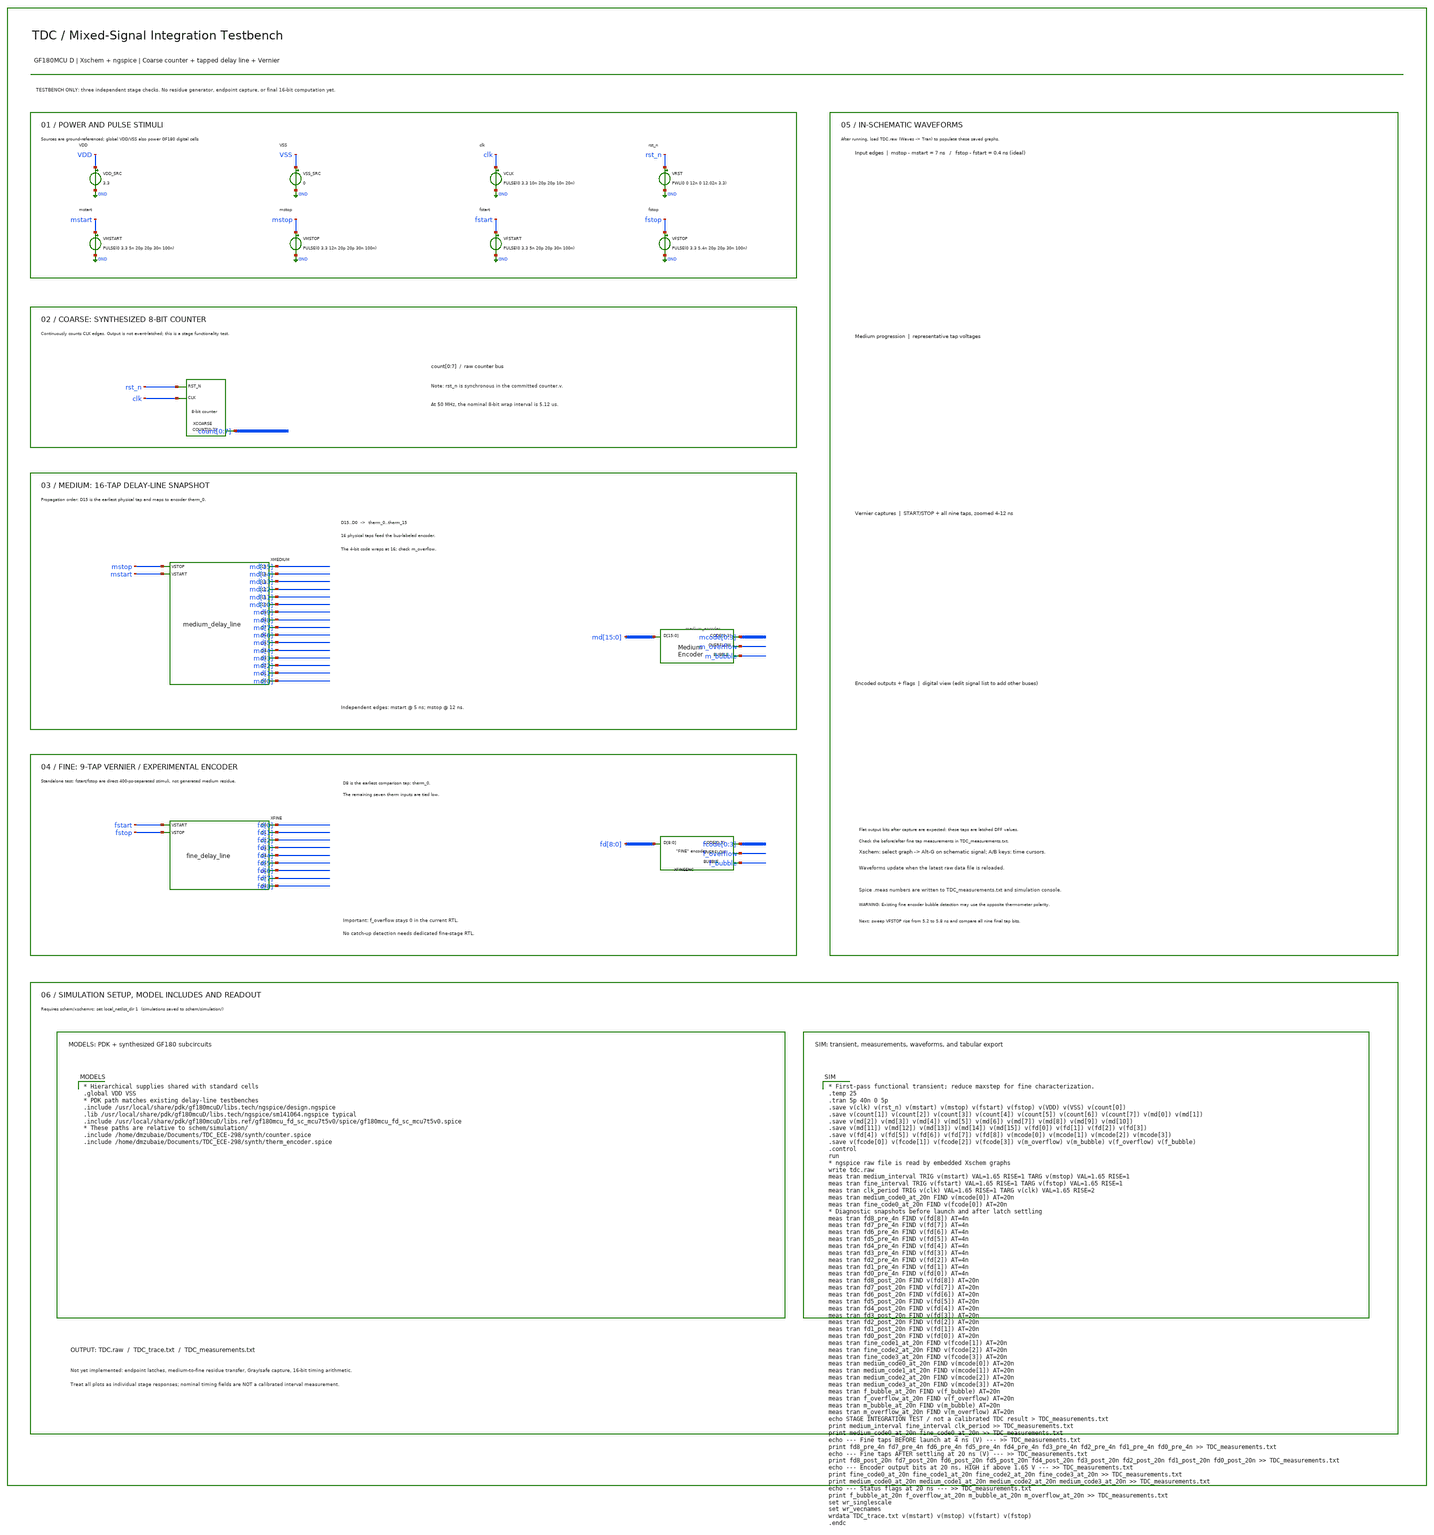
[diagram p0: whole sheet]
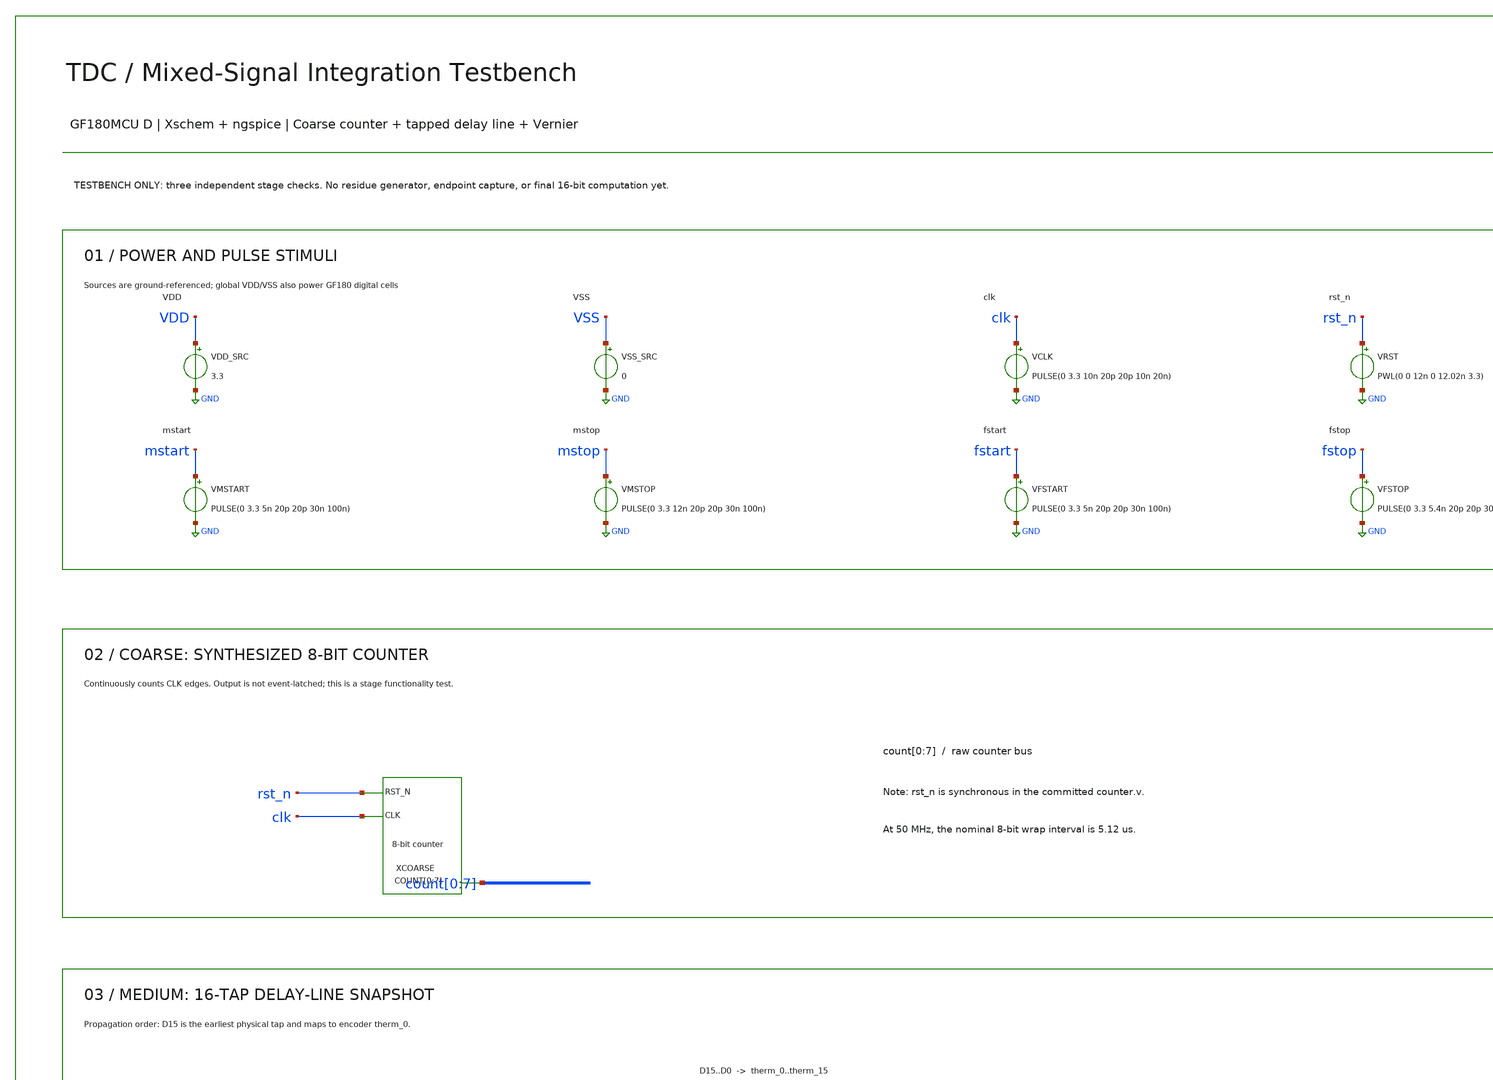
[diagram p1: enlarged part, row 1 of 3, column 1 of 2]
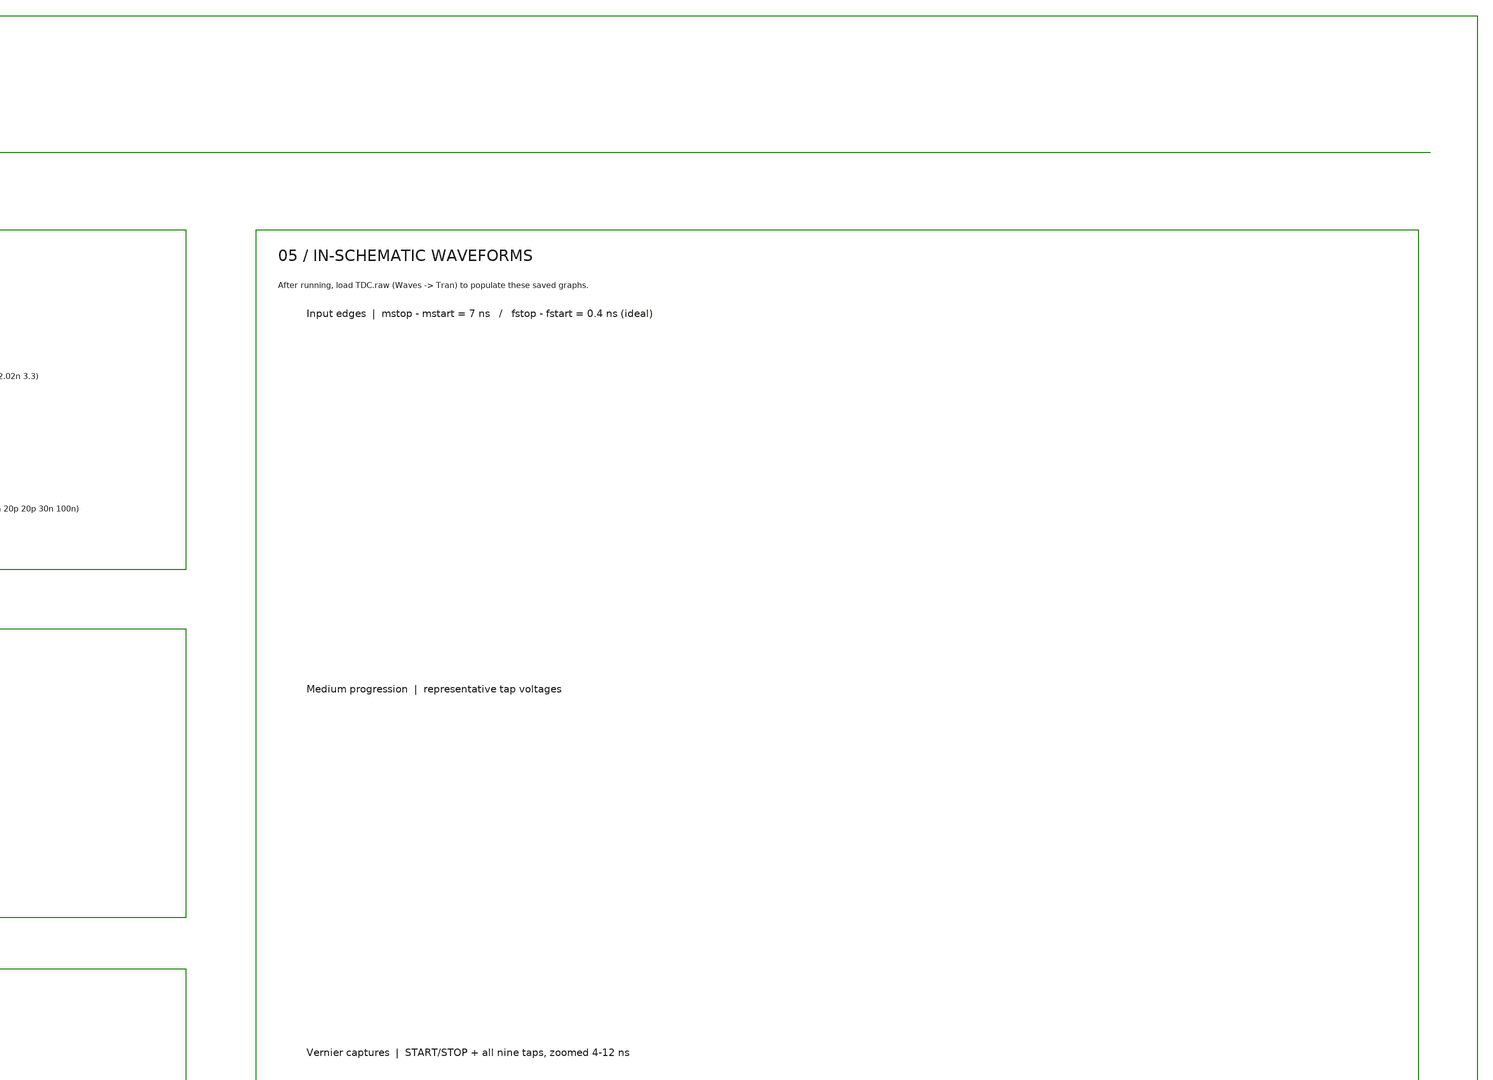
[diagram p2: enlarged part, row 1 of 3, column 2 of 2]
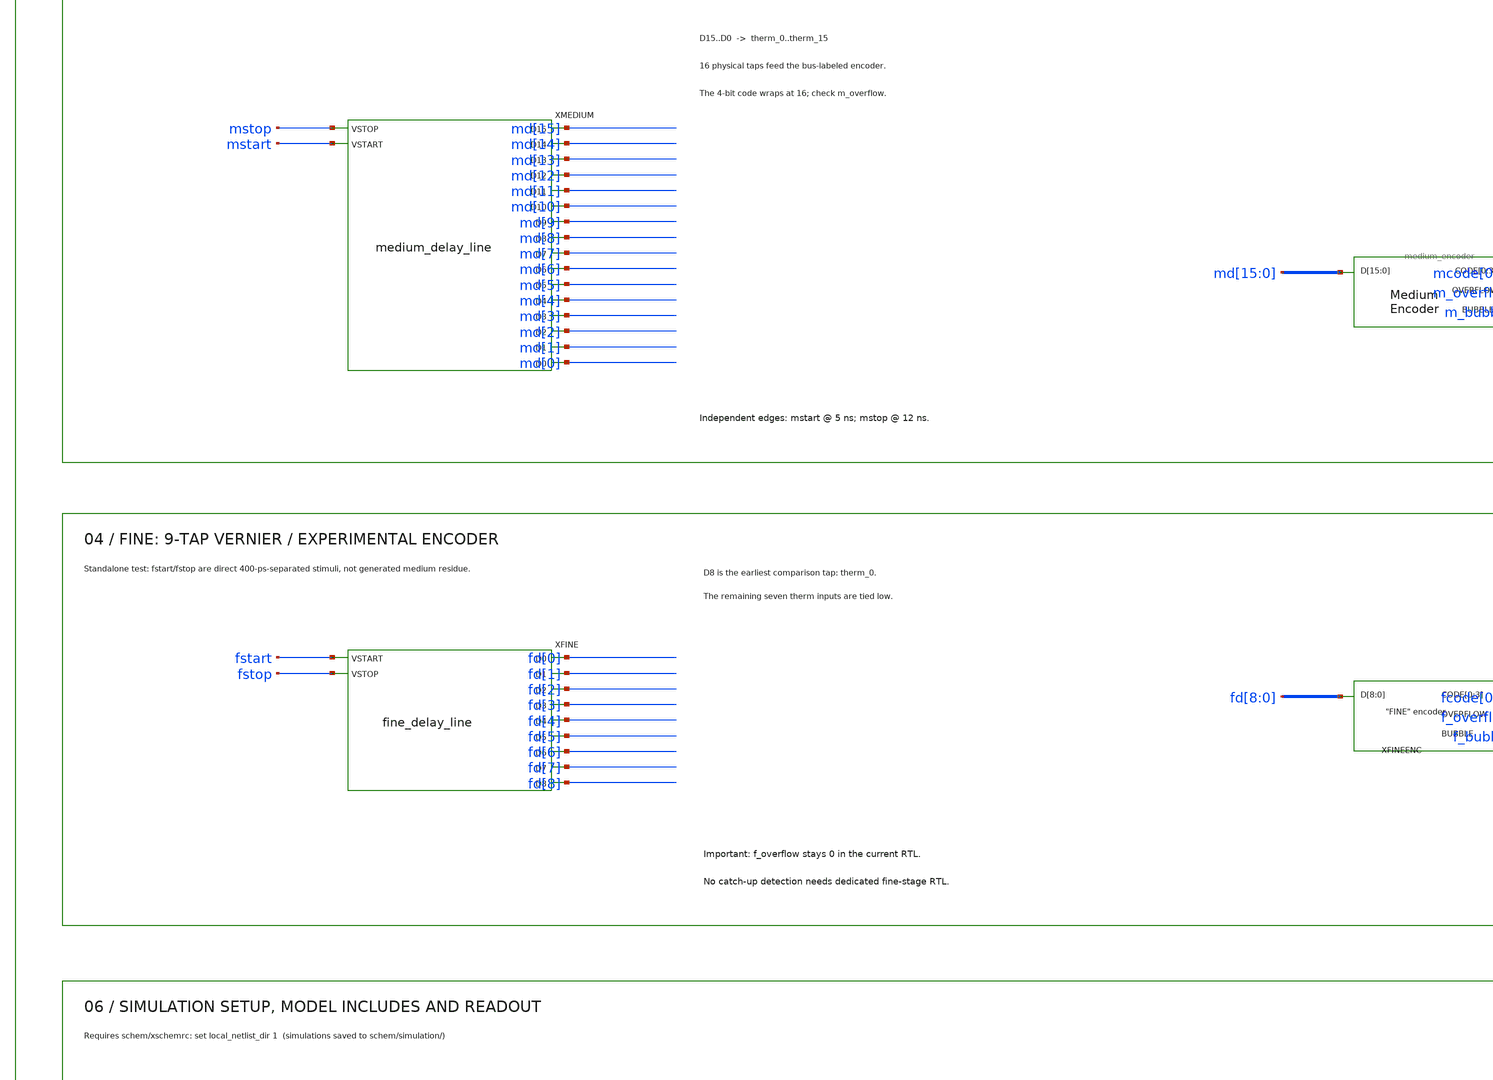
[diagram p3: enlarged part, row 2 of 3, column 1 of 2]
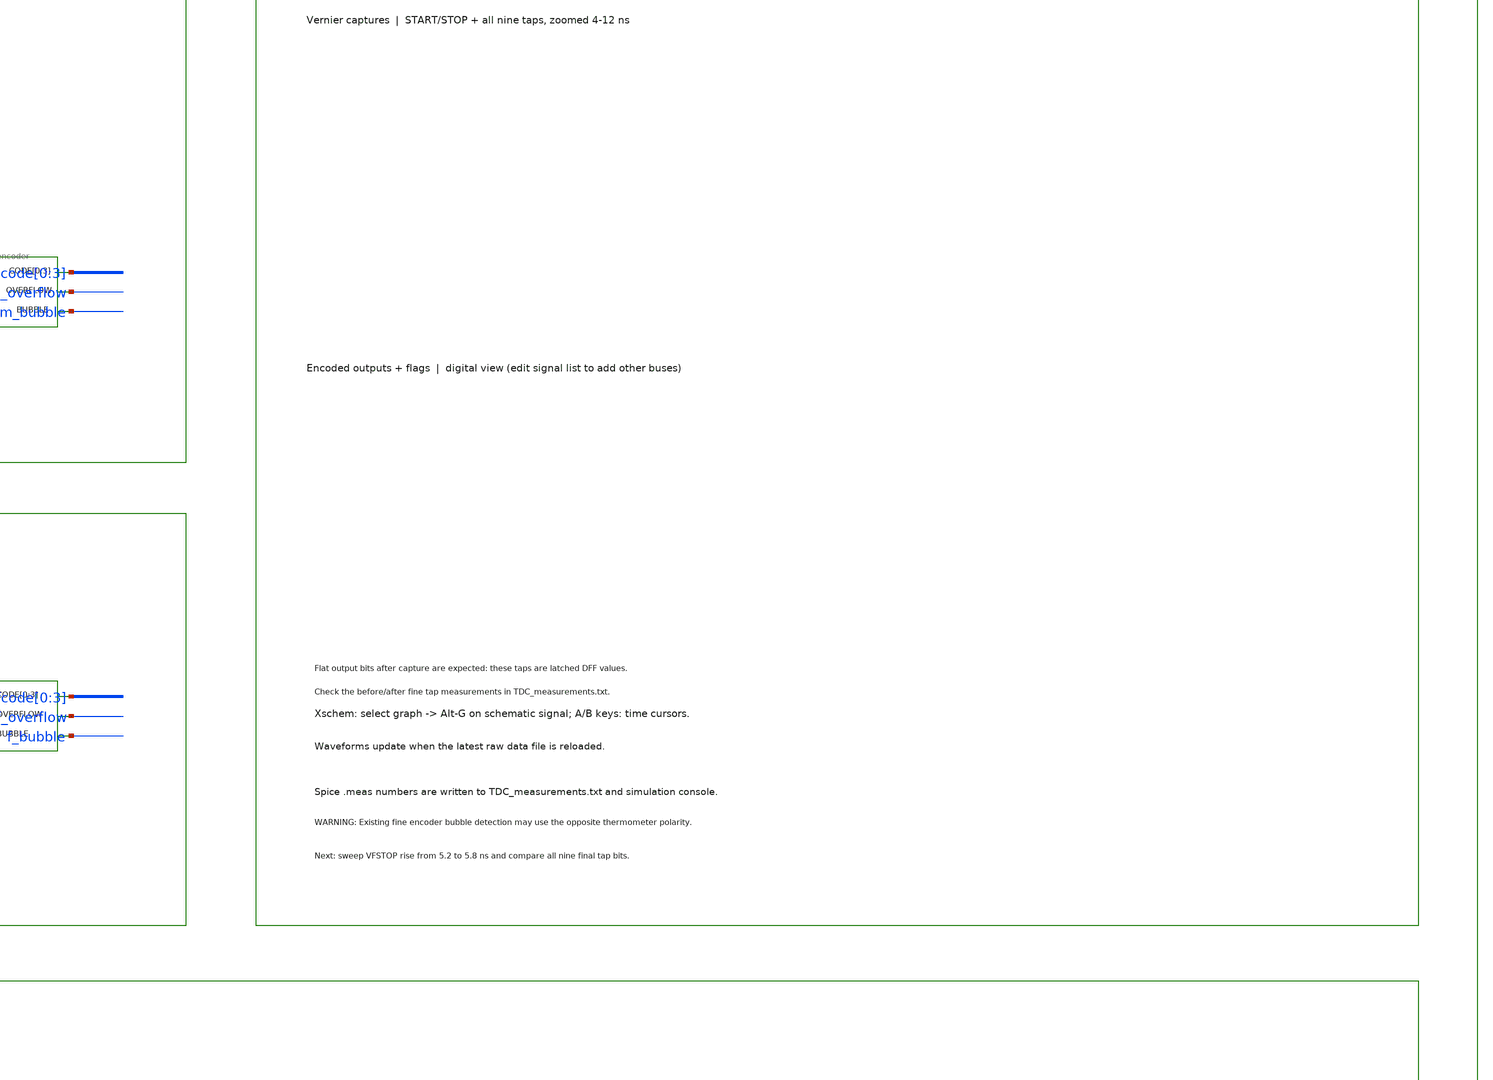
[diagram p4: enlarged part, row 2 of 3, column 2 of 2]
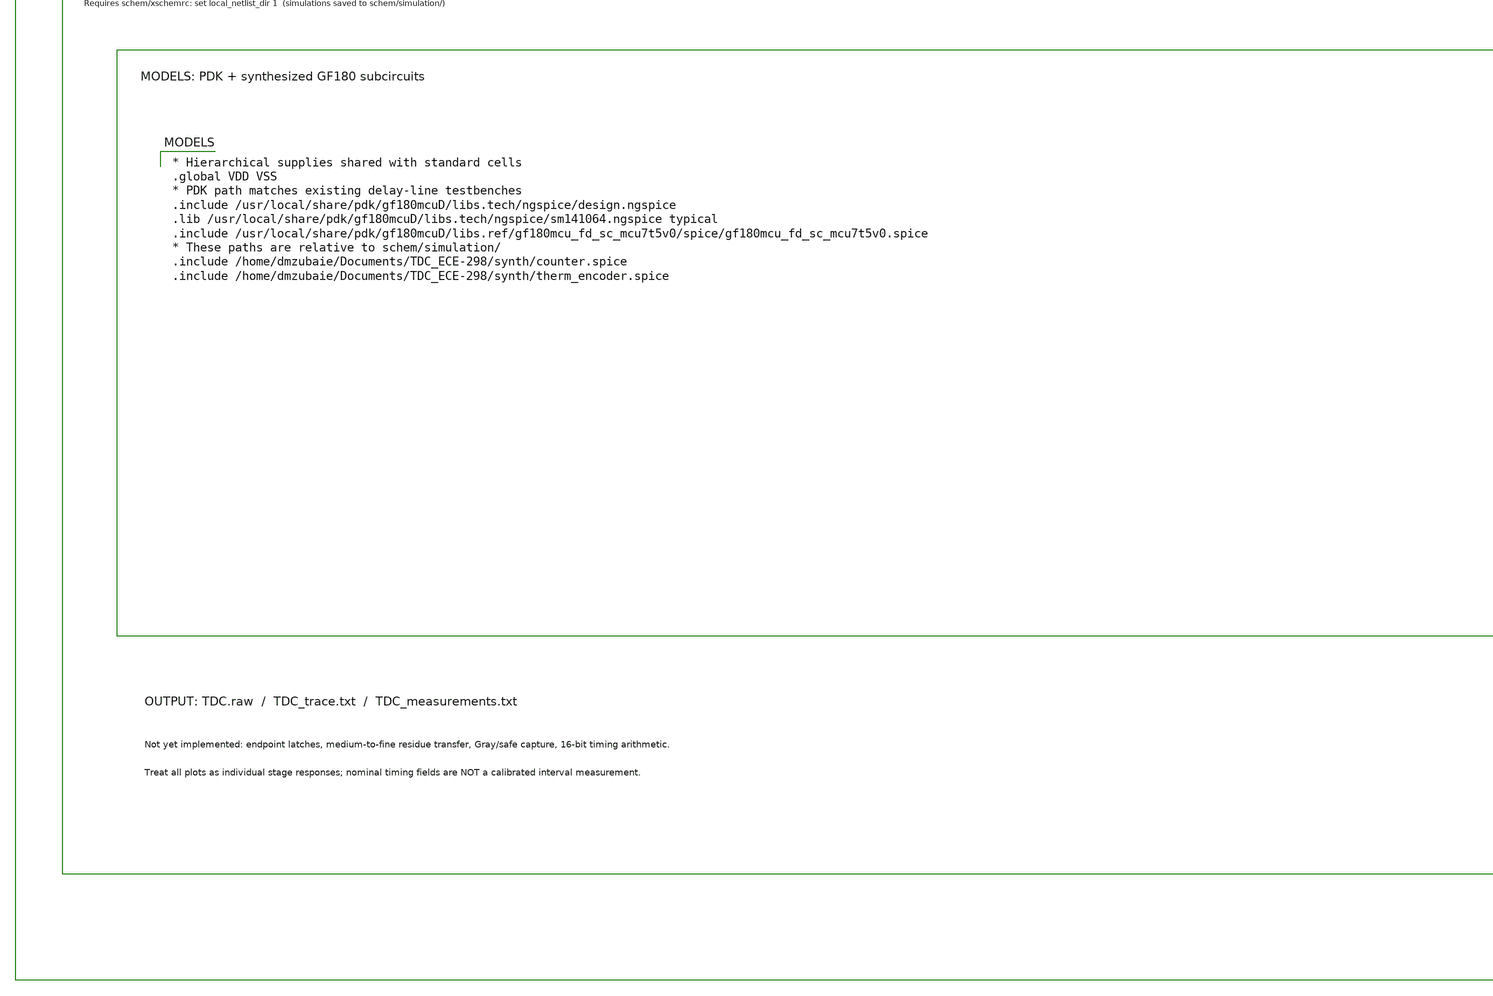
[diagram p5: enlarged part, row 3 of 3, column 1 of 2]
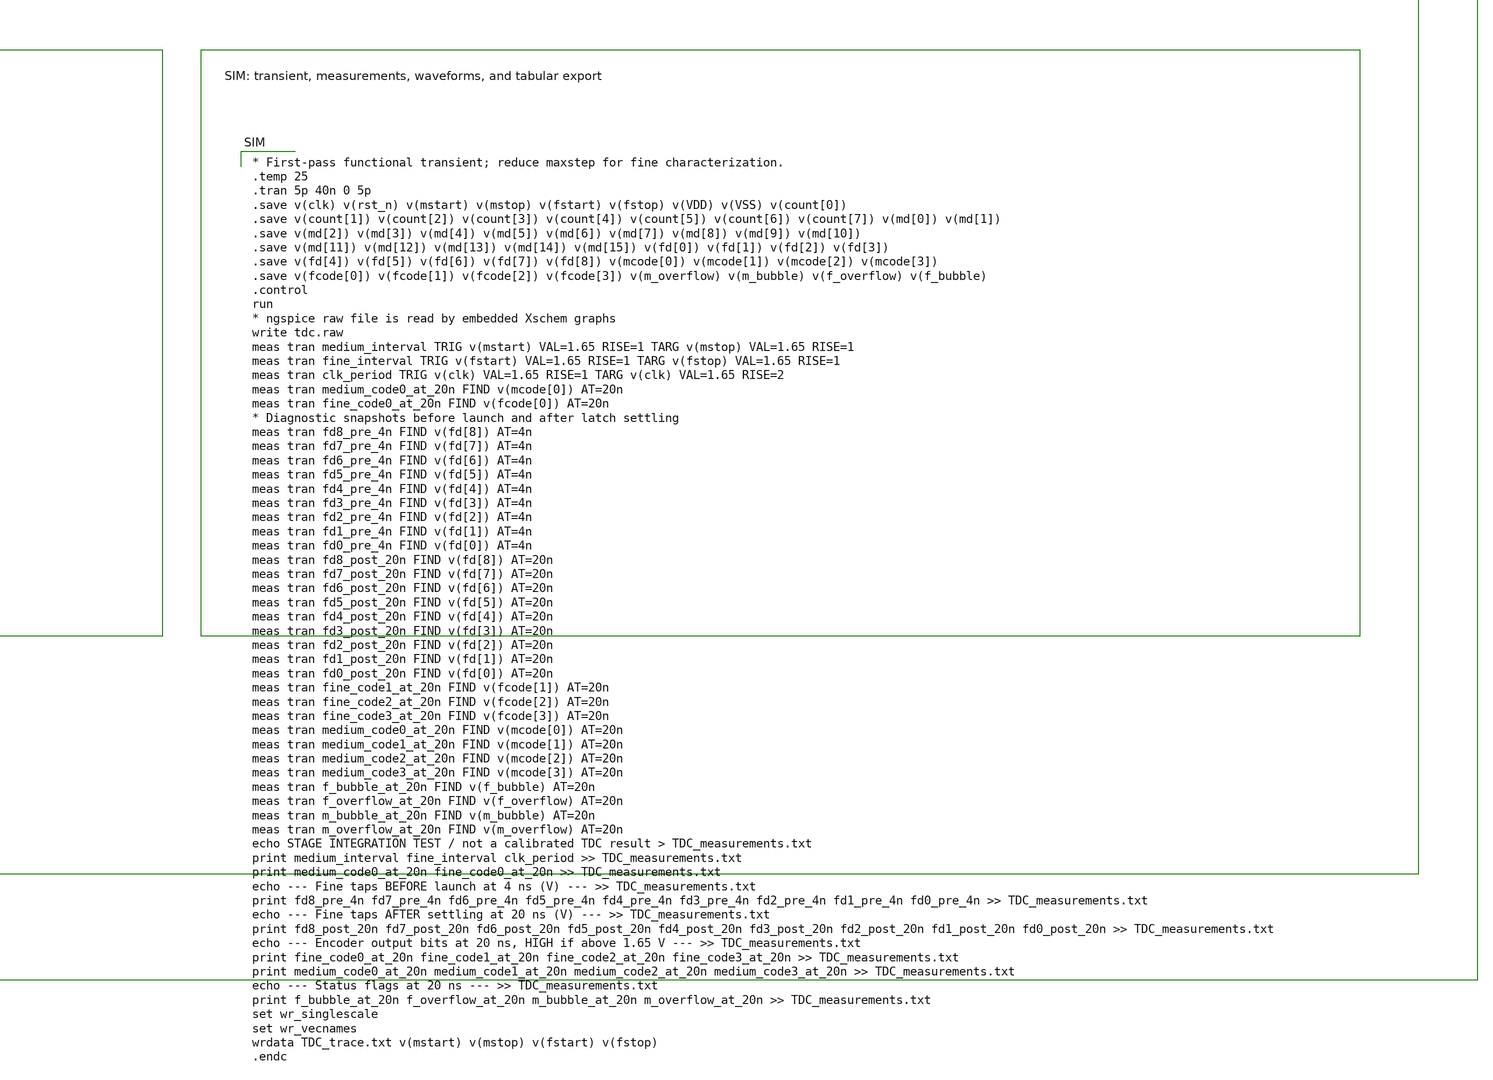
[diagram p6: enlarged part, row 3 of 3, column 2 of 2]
** sch_path: schem/tdc.sch
**.subckt tdc
VDD_SRC VDD GND 3.3
VSS_SRC VSS GND 0
VCLK clk GND PULSE(0 3.3 10n 20p 20p 10n 20n)
VRST rst_n GND PWL(0 0 12n 0 12.02n 3.3)
VMSTART mstart GND PULSE(0 3.3 5n 20p 20p 30n 100n)
VMSTOP mstop GND PULSE(0 3.3 12n 20p 20p 30n 100n)
VFSTART fstart GND PULSE(0 3.3 5n 20p 20p 30n 100n)
VFSTOP fstop GND PULSE(0 3.3 5.4n 20p 20p 30n 100n)
XCOARSE clk rst_n count[0] count[1] count[2] count[3] count[4] count[5] count[6] count[7] VDD VSS
+ counter
XMEDIUM mstop md[15] md[2] md[13] md[12] md[11] md[10] md[9] md[8] md[7] md[6] md[5] md[4] md[3]
+ md[14] md[1] md[0] mstart medium_delay_line
XMEDENC md[15] md[14] md[13] md[12] md[11] md[10] md[9] md[8] md[7] md[6] md[5] md[4] md[3] md[2]
+ md[1] md[0] mcode[0] mcode[1] mcode[2] mcode[3] m_overflow m_bubble VDD VSS therm_encoder
XFINE fstart fd[0] fd[5] fd[2] fd[3] fd[4] fd[1] fd[6] fd[7] fd[8] fstop fine_delay_line
XFINEENC fd[8] fd[7] fd[6] fd[5] fd[4] fd[3] fd[2] fd[1] fd[0] VSS VSS VSS VSS VSS VSS VSS fcode[0]
+ fcode[1] fcode[2] fcode[3] f_overflow f_bubble VDD VSS therm_encoder
**** begin user architecture code

* Hierarchical supplies shared with standard cells
.global VDD VSS
* PDK path matches existing delay-line testbenches
.include /usr/local/share/pdk/gf180mcuD/libs.tech/ngspice/design.ngspice
.lib /usr/local/share/pdk/gf180mcuD/libs.tech/ngspice/sm141064.ngspice typical
.include /usr/local/share/pdk/gf180mcuD/libs.ref/gf180mcu_fd_sc_mcu7t5v0/spice/gf180mcu_fd_sc_mcu7t5v0.spice
* These paths are relative to schem/simulation/
.include /home/dmzubaie/Documents/TDC_ECE-298/synth/counter.spice
.include /home/dmzubaie/Documents/TDC_ECE-298/synth/therm_encoder.spice


* First-pass functional transient; reduce maxstep for fine characterization.
.temp 25
.tran 5p 40n 0 5p
.save v(clk) v(rst_n) v(mstart) v(mstop) v(fstart) v(fstop) v(VDD) v(VSS) v(count[0])
.save v(count[1]) v(count[2]) v(count[3]) v(count[4]) v(count[5]) v(count[6]) v(count[7]) v(md[0]) v(md[1])
.save v(md[2]) v(md[3]) v(md[4]) v(md[5]) v(md[6]) v(md[7]) v(md[8]) v(md[9]) v(md[10])
.save v(md[11]) v(md[12]) v(md[13]) v(md[14]) v(md[15]) v(fd[0]) v(fd[1]) v(fd[2]) v(fd[3])
.save v(fd[4]) v(fd[5]) v(fd[6]) v(fd[7]) v(fd[8]) v(mcode[0]) v(mcode[1]) v(mcode[2]) v(mcode[3])
.save v(fcode[0]) v(fcode[1]) v(fcode[2]) v(fcode[3]) v(m_overflow) v(m_bubble) v(f_overflow) v(f_bubble)
.control
run
* ngspice raw file is read by embedded Xschem graphs
write tdc.raw
meas tran medium_interval TRIG v(mstart) VAL=1.65 RISE=1 TARG v(mstop) VAL=1.65 RISE=1
meas tran fine_interval TRIG v(fstart) VAL=1.65 RISE=1 TARG v(fstop) VAL=1.65 RISE=1
meas tran clk_period TRIG v(clk) VAL=1.65 RISE=1 TARG v(clk) VAL=1.65 RISE=2
meas tran medium_code0_at_20n FIND v(mcode[0]) AT=20n
meas tran fine_code0_at_20n FIND v(fcode[0]) AT=20n
* Diagnostic snapshots before launch and after latch settling
meas tran fd8_pre_4n FIND v(fd[8]) AT=4n
meas tran fd7_pre_4n FIND v(fd[7]) AT=4n
meas tran fd6_pre_4n FIND v(fd[6]) AT=4n
meas tran fd5_pre_4n FIND v(fd[5]) AT=4n
meas tran fd4_pre_4n FIND v(fd[4]) AT=4n
meas tran fd3_pre_4n FIND v(fd[3]) AT=4n
meas tran fd2_pre_4n FIND v(fd[2]) AT=4n
meas tran fd1_pre_4n FIND v(fd[1]) AT=4n
meas tran fd0_pre_4n FIND v(fd[0]) AT=4n
meas tran fd8_post_20n FIND v(fd[8]) AT=20n
meas tran fd7_post_20n FIND v(fd[7]) AT=20n
meas tran fd6_post_20n FIND v(fd[6]) AT=20n
meas tran fd5_post_20n FIND v(fd[5]) AT=20n
meas tran fd4_post_20n FIND v(fd[4]) AT=20n
meas tran fd3_post_20n FIND v(fd[3]) AT=20n
meas tran fd2_post_20n FIND v(fd[2]) AT=20n
meas tran fd1_post_20n FIND v(fd[1]) AT=20n
meas tran fd0_post_20n FIND v(fd[0]) AT=20n
meas tran fine_code1_at_20n FIND v(fcode[1]) AT=20n
meas tran fine_code2_at_20n FIND v(fcode[2]) AT=20n
meas tran fine_code3_at_20n FIND v(fcode[3]) AT=20n
meas tran medium_code0_at_20n FIND v(mcode[0]) AT=20n
meas tran medium_code1_at_20n FIND v(mcode[1]) AT=20n
meas tran medium_code2_at_20n FIND v(mcode[2]) AT=20n
meas tran medium_code3_at_20n FIND v(mcode[3]) AT=20n
meas tran f_bubble_at_20n FIND v(f_bubble) AT=20n
meas tran f_overflow_at_20n FIND v(f_overflow) AT=20n
meas tran m_bubble_at_20n FIND v(m_bubble) AT=20n
meas tran m_overflow_at_20n FIND v(m_overflow) AT=20n
echo STAGE INTEGRATION TEST / not a calibrated TDC result > TDC_measurements.txt
print medium_interval fine_interval clk_period >> TDC_measurements.txt
print medium_code0_at_20n fine_code0_at_20n >> TDC_measurements.txt
echo --- Fine taps BEFORE launch at 4 ns (V) --- >> TDC_measurements.txt
print fd8_pre_4n fd7_pre_4n fd6_pre_4n fd5_pre_4n fd4_pre_4n fd3_pre_4n fd2_pre_4n fd1_pre_4n
+ fd0_pre_4n >> TDC_measurements.txt
echo --- Fine taps AFTER settling at 20 ns (V) --- >> TDC_measurements.txt
print fd8_post_20n fd7_post_20n fd6_post_20n fd5_post_20n fd4_post_20n fd3_post_20n fd2_post_20n
+ fd1_post_20n fd0_post_20n >> TDC_measurements.txt
echo --- Encoder output bits at 20 ns, HIGH if above 1.65 V --- >> TDC_measurements.txt
print fine_code0_at_20n fine_code1_at_20n fine_code2_at_20n fine_code3_at_20n >>
+ TDC_measurements.txt
print medium_code0_at_20n medium_code1_at_20n medium_code2_at_20n medium_code3_at_20n >>
+ TDC_measurements.txt
echo --- Status flags at 20 ns --- >> TDC_measurements.txt
print f_bubble_at_20n f_overflow_at_20n m_bubble_at_20n m_overflow_at_20n >> TDC_measurements.txt
set wr_singlescale
set wr_vecnames
wrdata TDC_trace.txt v(mstart) v(mstop) v(fstart) v(fstop)
.endc

**** end user architecture code
**.ends

* expanding   symbol:  medium_delay_line.sym # of pins=18
** sym_path: schem/medium_delay_line.sym
** sch_path: schem/medium_delay_line.sch
.subckt medium_delay_line VSTOP D15 D2 D13 D12 D11 D10 D9 D8 D7 D6 D5 D4 D3 D14 D1 D0 VSTART
*.ipin VSTOP
*.ipin VSTART
*.opin D15
*.opin D14
*.opin D13
*.opin D12
*.opin D11
*.opin D10
*.opin D9
*.opin D8
*.opin D7
*.opin D6
*.opin D5
*.opin D4
*.opin D3
*.opin D2
*.opin D1
*.opin D0
X1 net1 VSTOP D15 VDD VDD 0 0 gf180mcu_fd_sc_mcu7t5v0__dffq_4
X2 VSTART net1 VDD VDD 0 0 gf180mcu_fd_sc_mcu7t5v0__dlyc_1
X3 net2 VSTOP D14 VDD VDD 0 0 gf180mcu_fd_sc_mcu7t5v0__dffq_4
X4 net1 net2 VDD VDD 0 0 gf180mcu_fd_sc_mcu7t5v0__dlyc_1
X5 net3 VSTOP D13 VDD VDD 0 0 gf180mcu_fd_sc_mcu7t5v0__dffq_4
X6 net2 net3 VDD VDD 0 0 gf180mcu_fd_sc_mcu7t5v0__dlyc_1
X7 net4 VSTOP D12 VDD VDD 0 0 gf180mcu_fd_sc_mcu7t5v0__dffq_4
X8 net3 net4 VDD VDD 0 0 gf180mcu_fd_sc_mcu7t5v0__dlyc_1
X9 net5 VSTOP D11 VDD VDD 0 0 gf180mcu_fd_sc_mcu7t5v0__dffq_4
X10 net4 net5 VDD VDD 0 0 gf180mcu_fd_sc_mcu7t5v0__dlyc_1
X11 net6 VSTOP D10 VDD VDD 0 0 gf180mcu_fd_sc_mcu7t5v0__dffq_4
X12 net5 net6 VDD VDD 0 0 gf180mcu_fd_sc_mcu7t5v0__dlyc_1
X13 net7 VSTOP D9 VDD VDD 0 0 gf180mcu_fd_sc_mcu7t5v0__dffq_4
X14 net6 net7 VDD VDD 0 0 gf180mcu_fd_sc_mcu7t5v0__dlyc_1
X15 net8 VSTOP D8 VDD VDD 0 0 gf180mcu_fd_sc_mcu7t5v0__dffq_4
X16 net7 net8 VDD VDD 0 0 gf180mcu_fd_sc_mcu7t5v0__dlyc_1
X17 net8 VSTOP D7 VDD VDD 0 0 gf180mcu_fd_sc_mcu7t5v0__dffq_4
X18 net9 VSTOP D6 VDD VDD 0 0 gf180mcu_fd_sc_mcu7t5v0__dffq_4
X19 net8 net9 VDD VDD 0 0 gf180mcu_fd_sc_mcu7t5v0__dlyc_1
X20 net10 VSTOP D5 VDD VDD 0 0 gf180mcu_fd_sc_mcu7t5v0__dffq_4
X21 net9 net10 VDD VDD 0 0 gf180mcu_fd_sc_mcu7t5v0__dlyc_1
X22 net11 VSTOP D4 VDD VDD 0 0 gf180mcu_fd_sc_mcu7t5v0__dffq_4
X23 net10 net11 VDD VDD 0 0 gf180mcu_fd_sc_mcu7t5v0__dlyc_1
X24 net12 VSTOP D3 VDD VDD 0 0 gf180mcu_fd_sc_mcu7t5v0__dffq_4
X25 net11 net12 VDD VDD 0 0 gf180mcu_fd_sc_mcu7t5v0__dlyc_1
X26 net13 VSTOP D2 VDD VDD 0 0 gf180mcu_fd_sc_mcu7t5v0__dffq_4
X27 net12 net13 VDD VDD 0 0 gf180mcu_fd_sc_mcu7t5v0__dlyc_1
X28 net14 VSTOP D1 VDD VDD 0 0 gf180mcu_fd_sc_mcu7t5v0__dffq_4
X29 net13 net14 VDD VDD 0 0 gf180mcu_fd_sc_mcu7t5v0__dlyc_1
X30 net15 VSTOP D0 VDD VDD 0 0 gf180mcu_fd_sc_mcu7t5v0__dffq_4
X31 net14 net15 VDD VDD 0 0 gf180mcu_fd_sc_mcu7t5v0__dlyc_1
.ends


* expanding   symbol:  fine_delay_line.sym # of pins=11
** sym_path: schem/fine_delay_line.sym
** sch_path: schem/fine_delay_line.sch
.subckt fine_delay_line VSTART D0 D5 D2 D3 D4 D1 D6 D7 D8 VSTOP
*.ipin VSTART
*.ipin VSTOP
*.opin D0
*.opin D1
*.opin D2
*.opin D3
*.opin D4
*.opin D5
*.opin D6
*.opin D7
*.opin D8
X1 VSTART net1 VDD VDD 0 0 gf180mcu_fd_sc_mcu7t5v0__dlya_4
X2 VSTOP net2 VDD VDD 0 0 gf180mcu_fd_sc_mcu7t5v0__dlya_1
X3 net2 net1 D8 VDD VDD 0 0 gf180mcu_fd_sc_mcu7t5v0__dffq_1
X4 net1 net3 VDD VDD 0 0 gf180mcu_fd_sc_mcu7t5v0__dlya_4
X5 net2 net4 VDD VDD 0 0 gf180mcu_fd_sc_mcu7t5v0__dlya_1
X6 net4 net3 D7 VDD VDD 0 0 gf180mcu_fd_sc_mcu7t5v0__dffq_1
X7 net3 net5 VDD VDD 0 0 gf180mcu_fd_sc_mcu7t5v0__dlya_4
X8 net4 net6 VDD VDD 0 0 gf180mcu_fd_sc_mcu7t5v0__dlya_1
X9 net6 net5 D6 VDD VDD 0 0 gf180mcu_fd_sc_mcu7t5v0__dffq_1
X10 net5 net7 VDD VDD 0 0 gf180mcu_fd_sc_mcu7t5v0__dlya_4
X11 net6 net8 VDD VDD 0 0 gf180mcu_fd_sc_mcu7t5v0__dlya_1
X12 net8 net7 D5 VDD VDD 0 0 gf180mcu_fd_sc_mcu7t5v0__dffq_1
X13 net7 net9 VDD VDD 0 0 gf180mcu_fd_sc_mcu7t5v0__dlya_4
X14 net8 net10 VDD VDD 0 0 gf180mcu_fd_sc_mcu7t5v0__dlya_1
X15 net10 net9 D4 VDD VDD 0 0 gf180mcu_fd_sc_mcu7t5v0__dffq_1
X16 net9 net11 VDD VDD 0 0 gf180mcu_fd_sc_mcu7t5v0__dlya_4
X17 net10 net12 VDD VDD 0 0 gf180mcu_fd_sc_mcu7t5v0__dlya_1
X18 net12 net11 D3 VDD VDD 0 0 gf180mcu_fd_sc_mcu7t5v0__dffq_1
X19 net11 net13 VDD VDD 0 0 gf180mcu_fd_sc_mcu7t5v0__dlya_4
X20 net12 net14 VDD VDD 0 0 gf180mcu_fd_sc_mcu7t5v0__dlya_1
X21 net14 net13 D2 VDD VDD 0 0 gf180mcu_fd_sc_mcu7t5v0__dffq_1
X22 net13 net15 VDD VDD 0 0 gf180mcu_fd_sc_mcu7t5v0__dlya_4
X23 net14 net16 VDD VDD 0 0 gf180mcu_fd_sc_mcu7t5v0__dlya_1
X24 net16 net15 D1 VDD VDD 0 0 gf180mcu_fd_sc_mcu7t5v0__dffq_1
X25 net15 net17 VDD VDD 0 0 gf180mcu_fd_sc_mcu7t5v0__dlya_4
X26 net16 net18 VDD VDD 0 0 gf180mcu_fd_sc_mcu7t5v0__dlya_1
X27 net18 net17 D0 VDD VDD 0 0 gf180mcu_fd_sc_mcu7t5v0__dffq_1
.ends

.GLOBAL GND
.end
